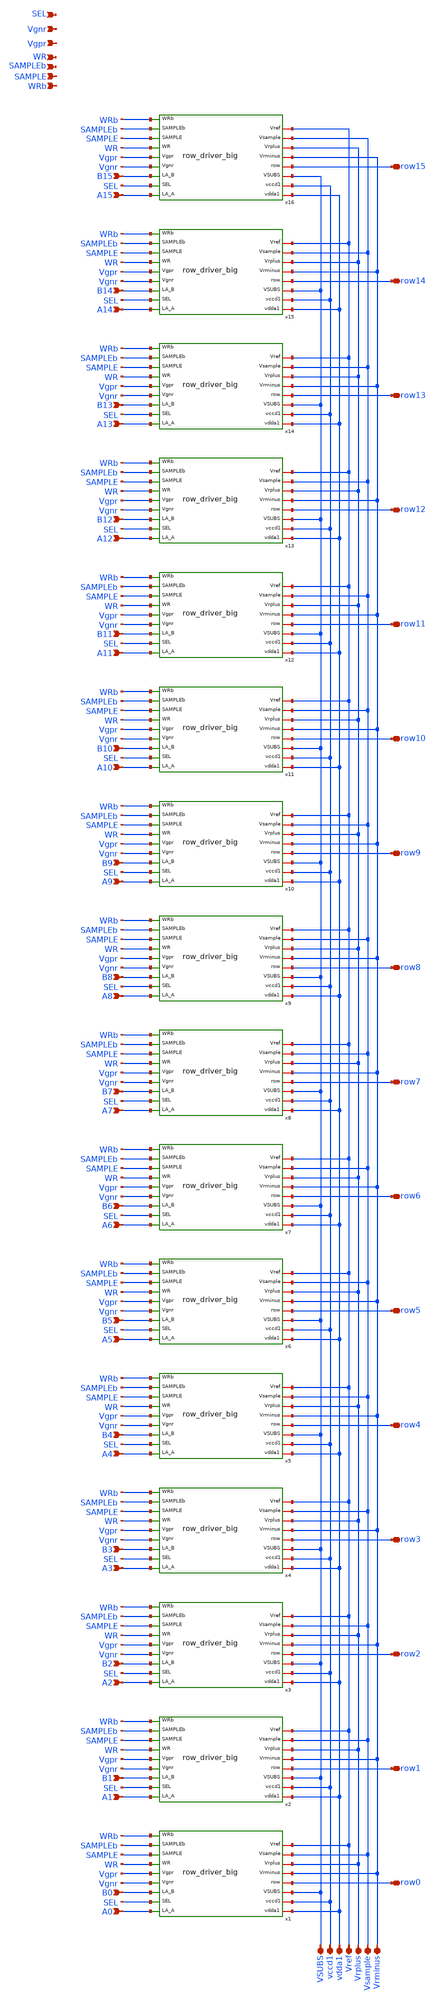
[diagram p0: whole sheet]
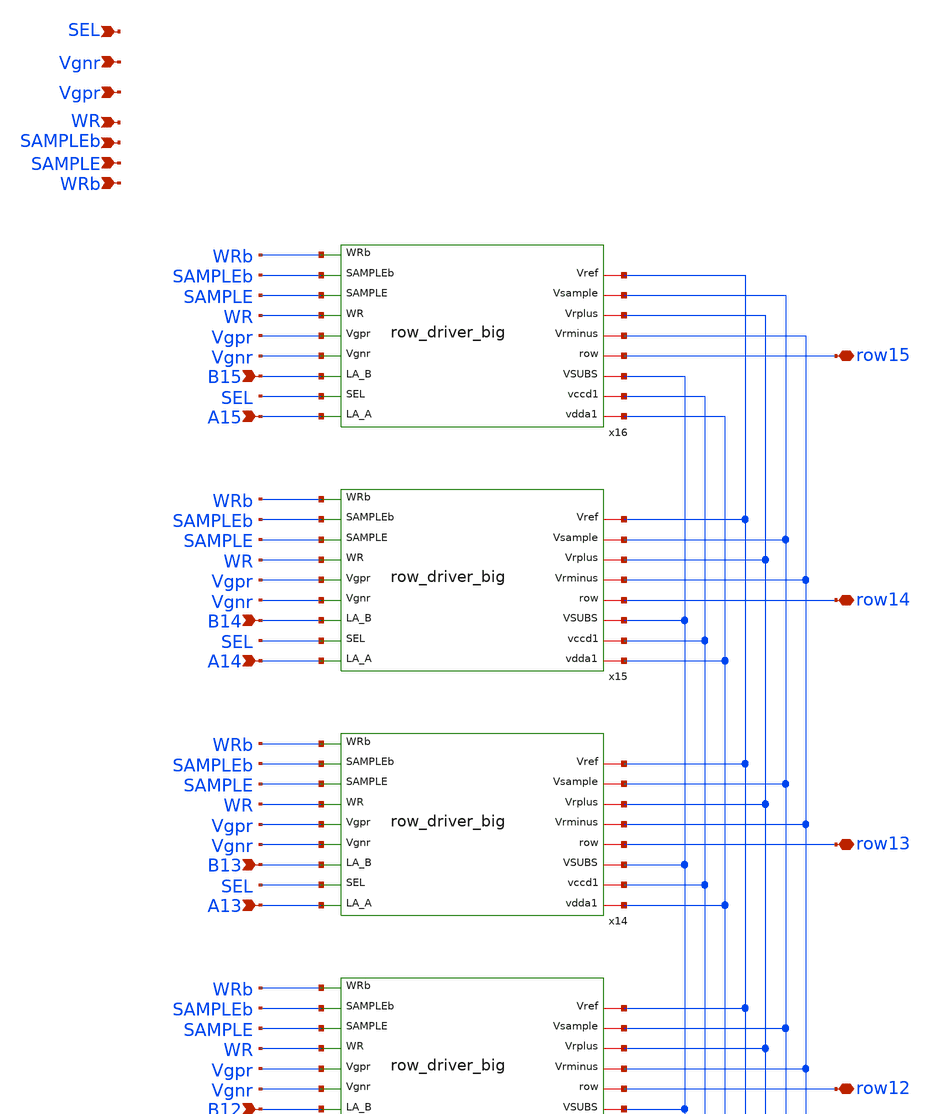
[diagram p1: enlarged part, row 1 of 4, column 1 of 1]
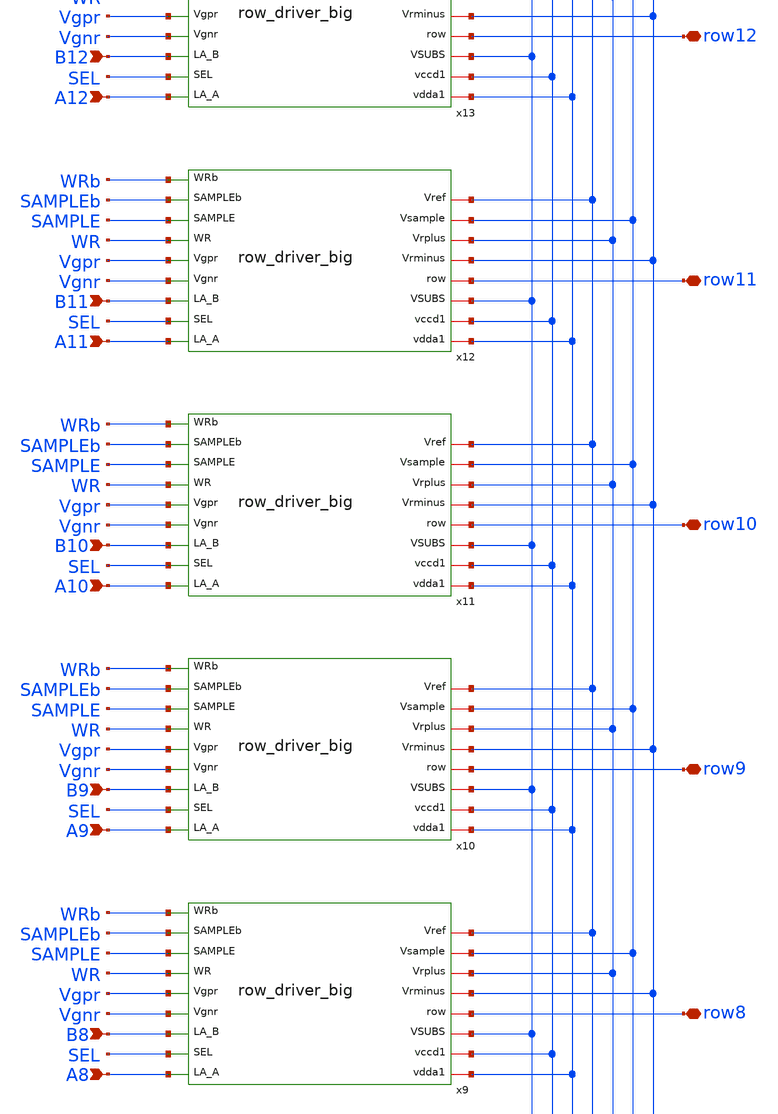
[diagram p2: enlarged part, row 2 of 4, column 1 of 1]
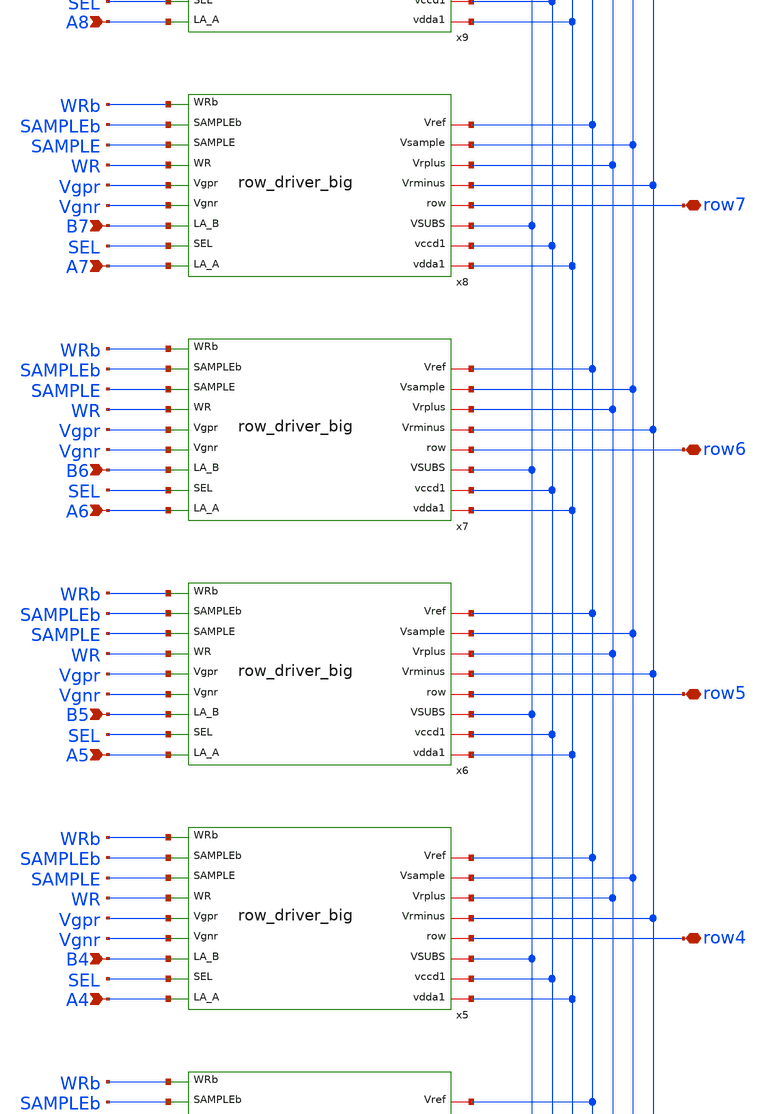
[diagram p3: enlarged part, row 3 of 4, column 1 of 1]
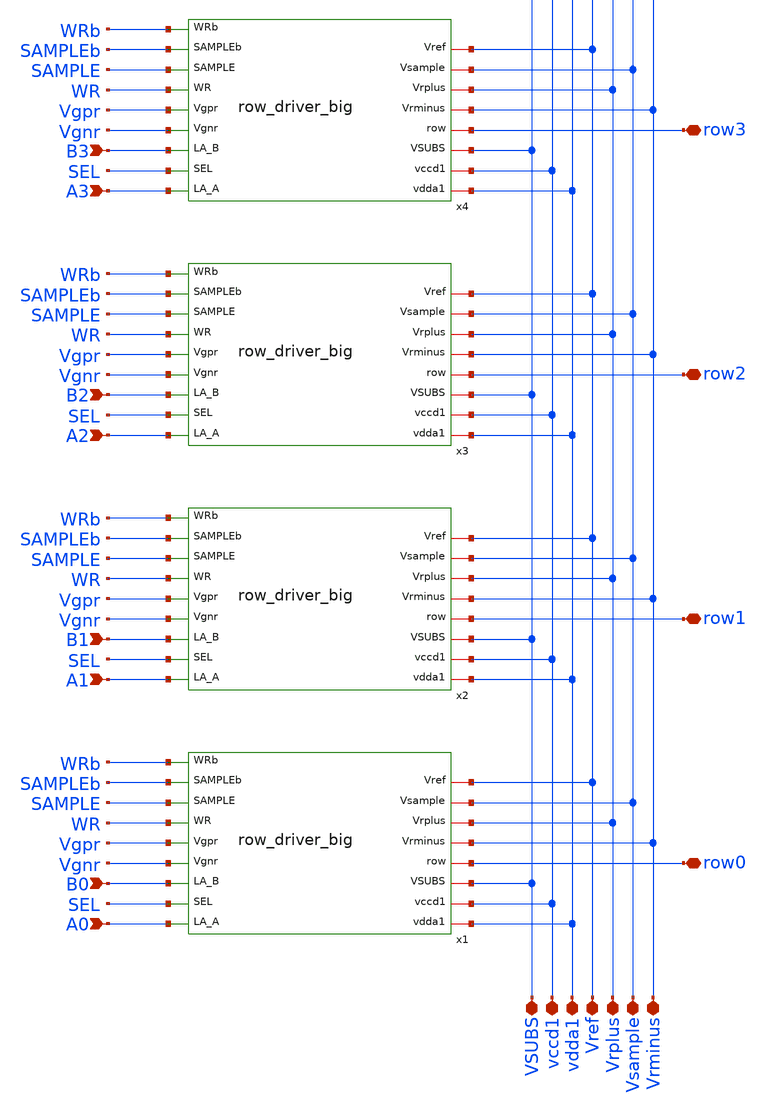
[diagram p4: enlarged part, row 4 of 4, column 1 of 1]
** sch_path: xschem/row_drivers_16x1.sch
**.subckt row_drivers_16x1 vdda1 VSUBS Vref Vrplus Vrminus vccd1 row0 A0 B0 row1 A1 B1 row2 A2 B2
*+ row3 row4 A3 B3 A4 B4 row5 A5 B5 row6 A6 B6 row7 A7 B7 row8 A8 B8 row9 A9 B9 row10 A10 B10 row11 row12
*+ A11 B11 A12 B12 row13 A13 B13 row14 A14 B14 row15 A15 B15 Vsample Vgpr Vgnr WR SAMPLEb WRb SAMPLE SEL
*.iopin vdda1
*.iopin VSUBS
*.iopin Vref
*.iopin Vrplus
*.iopin Vrminus
*.iopin vccd1
*.iopin row0
*.ipin A0
*.ipin B0
*.iopin row1
*.ipin A1
*.ipin B1
*.iopin row2
*.ipin A2
*.ipin B2
*.iopin row3
*.iopin row4
*.ipin A3
*.ipin B3
*.ipin A4
*.ipin B4
*.iopin row5
*.ipin A5
*.ipin B5
*.iopin row6
*.ipin A6
*.ipin B6
*.iopin row7
*.ipin A7
*.ipin B7
*.iopin row8
*.ipin A8
*.ipin B8
*.iopin row9
*.ipin A9
*.ipin B9
*.iopin row10
*.ipin A10
*.ipin B10
*.iopin row11
*.iopin row12
*.ipin A11
*.ipin B11
*.ipin A12
*.ipin B12
*.iopin row13
*.ipin A13
*.ipin B13
*.iopin row14
*.ipin A14
*.ipin B14
*.iopin row15
*.ipin A15
*.ipin B15
*.iopin Vsample
*.ipin Vgpr
*.ipin Vgnr
*.ipin WR
*.ipin SAMPLEb
*.ipin WRb
*.ipin SAMPLE
*.ipin SEL
x1 vdda1 vccd1 VSUBS row0 A0 SEL B0 Vgnr Vgpr Vrminus Vrplus Vsample WR SAMPLE SAMPLEb WRb Vref
+ row_driver_big
x2 vdda1 vccd1 VSUBS row1 A1 SEL B1 Vgnr Vgpr Vrminus Vrplus Vsample WR SAMPLE SAMPLEb WRb Vref
+ row_driver_big
x3 vdda1 vccd1 VSUBS row2 A2 SEL B2 Vgnr Vgpr Vrminus Vrplus Vsample WR SAMPLE SAMPLEb WRb Vref
+ row_driver_big
x4 vdda1 vccd1 VSUBS row3 A3 SEL B3 Vgnr Vgpr Vrminus Vrplus Vsample WR SAMPLE SAMPLEb WRb Vref
+ row_driver_big
x5 vdda1 vccd1 VSUBS row4 A4 SEL B4 Vgnr Vgpr Vrminus Vrplus Vsample WR SAMPLE SAMPLEb WRb Vref
+ row_driver_big
x6 vdda1 vccd1 VSUBS row5 A5 SEL B5 Vgnr Vgpr Vrminus Vrplus Vsample WR SAMPLE SAMPLEb WRb Vref
+ row_driver_big
x7 vdda1 vccd1 VSUBS row6 A6 SEL B6 Vgnr Vgpr Vrminus Vrplus Vsample WR SAMPLE SAMPLEb WRb Vref
+ row_driver_big
x8 vdda1 vccd1 VSUBS row7 A7 SEL B7 Vgnr Vgpr Vrminus Vrplus Vsample WR SAMPLE SAMPLEb WRb Vref
+ row_driver_big
x9 vdda1 vccd1 VSUBS row8 A8 SEL B8 Vgnr Vgpr Vrminus Vrplus Vsample WR SAMPLE SAMPLEb WRb Vref
+ row_driver_big
x10 vdda1 vccd1 VSUBS row9 A9 SEL B9 Vgnr Vgpr Vrminus Vrplus Vsample WR SAMPLE SAMPLEb WRb Vref
+ row_driver_big
x11 vdda1 vccd1 VSUBS row10 A10 SEL B10 Vgnr Vgpr Vrminus Vrplus Vsample WR SAMPLE SAMPLEb WRb Vref
+ row_driver_big
x12 vdda1 vccd1 VSUBS row11 A11 SEL B11 Vgnr Vgpr Vrminus Vrplus Vsample WR SAMPLE SAMPLEb WRb Vref
+ row_driver_big
x13 vdda1 vccd1 VSUBS row12 A12 SEL B12 Vgnr Vgpr Vrminus Vrplus Vsample WR SAMPLE SAMPLEb WRb Vref
+ row_driver_big
x14 vdda1 vccd1 VSUBS row13 A13 SEL B13 Vgnr Vgpr Vrminus Vrplus Vsample WR SAMPLE SAMPLEb WRb Vref
+ row_driver_big
x15 vdda1 vccd1 VSUBS row14 A14 SEL B14 Vgnr Vgpr Vrminus Vrplus Vsample WR SAMPLE SAMPLEb WRb Vref
+ row_driver_big
x16 vdda1 vccd1 VSUBS row15 A15 SEL B15 Vgnr Vgpr Vrminus Vrplus Vsample WR SAMPLE SAMPLEb WRb Vref
+ row_driver_big
**.ends
.end
